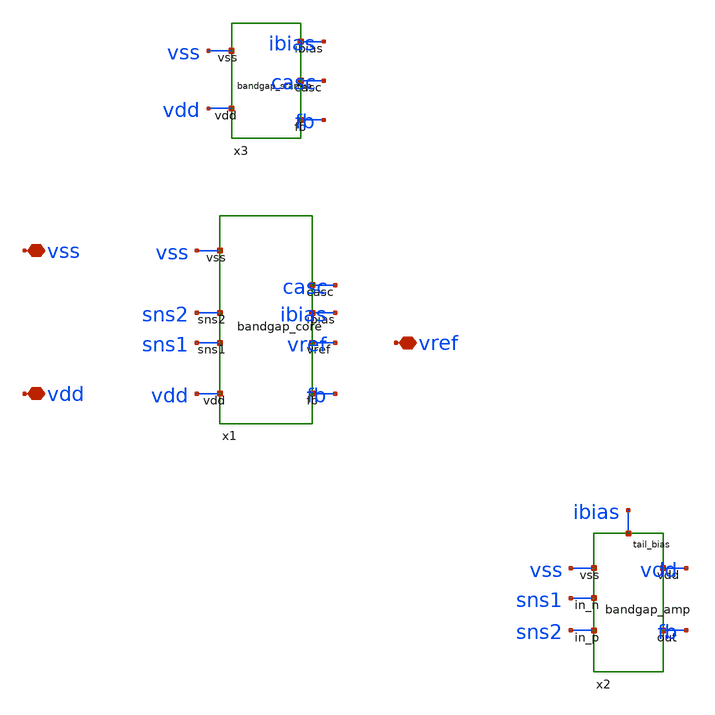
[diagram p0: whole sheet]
** sch_path: design/bandgap_top.sch
**.subckt bandgap_top vdd vss vref
*.iopin vdd
*.iopin vss
*.iopin vref
Xx1 vdd sns1 sns2 vss fb vref ibias casc bandgap_core
Xx2 sns2 sns1 vss fb vdd ibias bandgap_amp
Xx3 vdd vss fb casc ibias bandgap_startup
**.ends
.end
